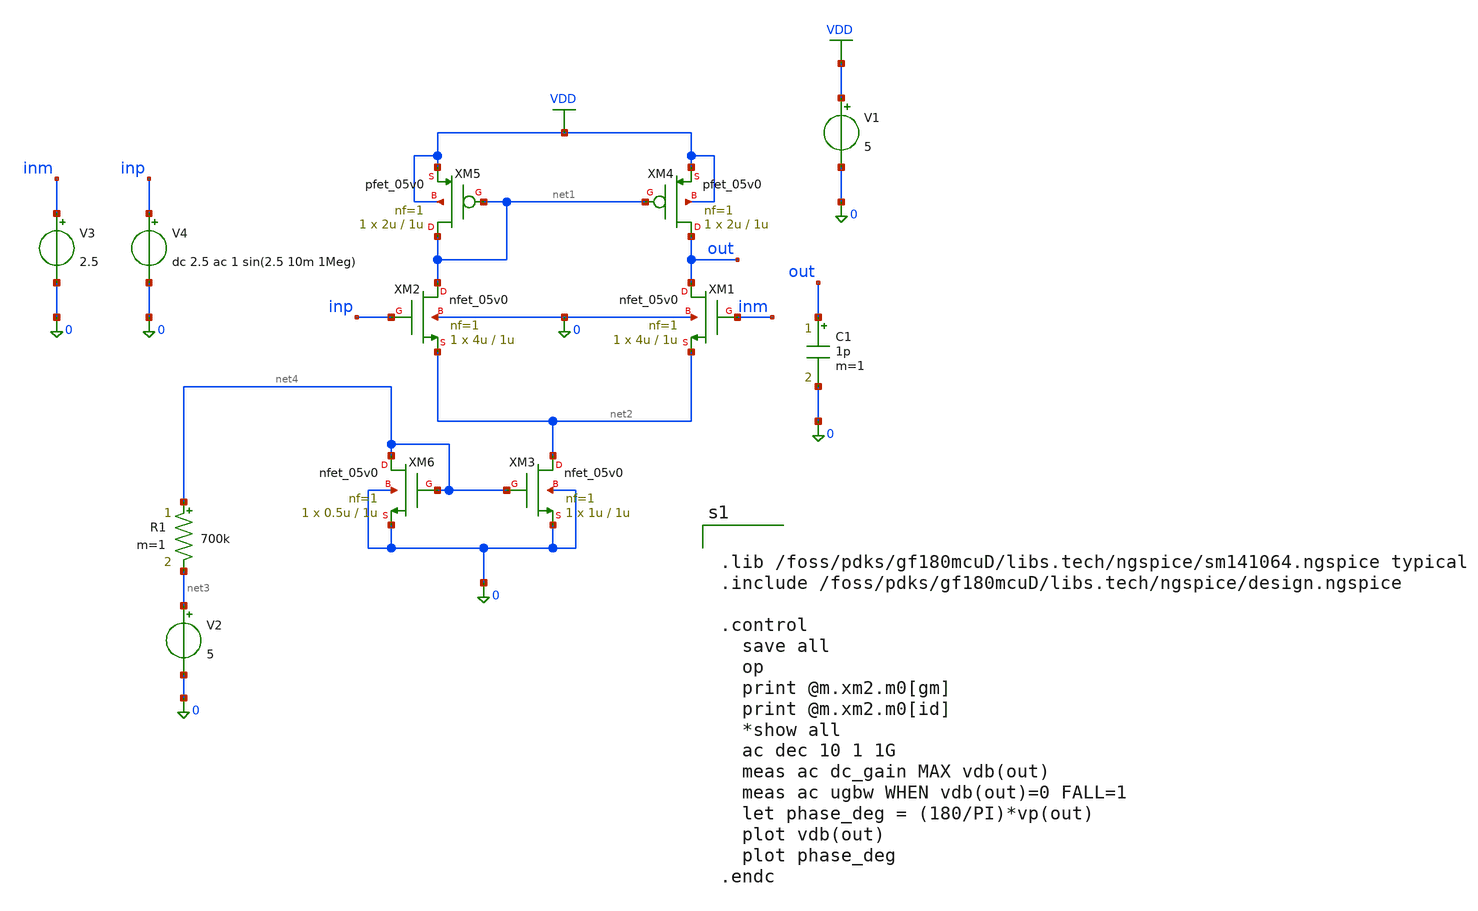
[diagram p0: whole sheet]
** sch_path: testcircuit.sch
**.subckt testcircuit
XM1 out inm net2 0 nfet_05v0 L=1u W=4u nf=1 ad='int((nf+1)/2) * W/nf * 0.18u' as='int((nf+2)/2) * W/nf * 0.18u'
+ pd='2*int((nf+1)/2) * (W/nf + 0.18u)' ps='2*int((nf+2)/2) * (W/nf + 0.18u)' nrd='0.18u / W' nrs='0.18u / W'
+ sa=0 sb=0 sd=0 m=1
XM2 net1 inp net2 0 nfet_05v0 L=1u W=4u nf=1 ad='int((nf+1)/2) * W/nf * 0.18u' as='int((nf+2)/2) * W/nf * 0.18u'
+ pd='2*int((nf+1)/2) * (W/nf + 0.18u)' ps='2*int((nf+2)/2) * (W/nf + 0.18u)' nrd='0.18u / W' nrs='0.18u / W'
+ sa=0 sb=0 sd=0 m=1
XM3 net2 net4 0 0 nfet_05v0 L=1u W=1u nf=1 ad='int((nf+1)/2) * W/nf * 0.18u' as='int((nf+2)/2) * W/nf * 0.18u'
+ pd='2*int((nf+1)/2) * (W/nf + 0.18u)' ps='2*int((nf+2)/2) * (W/nf + 0.18u)' nrd='0.18u / W' nrs='0.18u / W'
+ sa=0 sb=0 sd=0 m=1
XM4 out net1 VDD VDD pfet_05v0 L=1u W=2u nf=1 ad='int((nf+1)/2) * W/nf * 0.18u' as='int((nf+2)/2) * W/nf * 0.18u'
+ pd='2*int((nf+1)/2) * (W/nf + 0.18u)' ps='2*int((nf+2)/2) * (W/nf + 0.18u)' nrd='0.18u / W' nrs='0.18u / W'
+ sa=0 sb=0 sd=0 m=1
XM5 net1 net1 VDD VDD pfet_05v0 L=1u W=2u nf=1 ad='int((nf+1)/2) * W/nf * 0.18u' as='int((nf+2)/2) * W/nf * 0.18u'
+ pd='2*int((nf+1)/2) * (W/nf + 0.18u)' ps='2*int((nf+2)/2) * (W/nf + 0.18u)' nrd='0.18u / W' nrs='0.18u / W'
+ sa=0 sb=0 sd=0 m=1
V1 VDD 0 5
V3 inm 0 2.5
V4 inp 0 dc 2.5 ac 1 sin(2.5 10m 1Meg)
C1 out 0 1p m=1
R1 net4 net3 700k m=1
V2 net3 0 5
XM6 net4 net4 0 0 nfet_05v0 L=1u W=0.5u nf=1 ad='int((nf+1)/2) * W/nf * 0.18u' as='int((nf+2)/2) * W/nf * 0.18u'
+ pd='2*int((nf+1)/2) * (W/nf + 0.18u)' ps='2*int((nf+2)/2) * (W/nf + 0.18u)' nrd='0.18u / W' nrs='0.18u / W'
+ sa=0 sb=0 sd=0 m=1
**** begin user architecture code


.lib /foss/pdks/gf180mcuD/libs.tech/ngspice/sm141064.ngspice typical
.include /foss/pdks/gf180mcuD/libs.tech/ngspice/design.ngspice

.control
  save all
  op
  print @m.xm2.m0[gm]
  print @m.xm2.m0[id]
  *show all
  ac dec 10 1 1G
  meas ac dc_gain MAX vdb(out)
  meas ac ugbw WHEN vdb(out)=0 FALL=1
  let phase_deg = (180/PI)*vp(out)
  plot vdb(out)
  plot phase_deg
.endc


**** end user architecture code
**.ends
.GLOBAL VDD
.end
